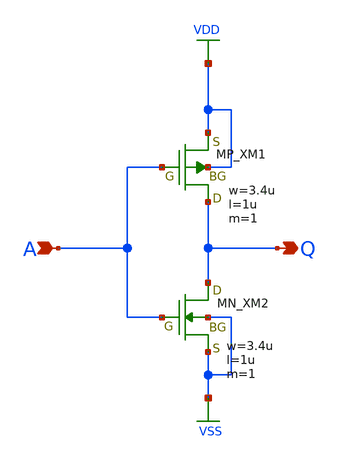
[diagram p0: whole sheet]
** sch_path: cmos_inverter.sch
**.subckt cmos_inverter A Q
*.ipin A
*.opin Q
XM1 Q A VDD VDD PMOS w=3.4u l=1u as=0 ad=0 ps=0 pd=0 nrd=0 nrs=0 m=1
XM2 Q A VSS VSS NMOS w=3.4u l=1u as=0 ad=0 ps=0 pd=0 nrd=0 nrs=0 m=1
**.ends
.GLOBAL VDD
.GLOBAL VSS
.end
